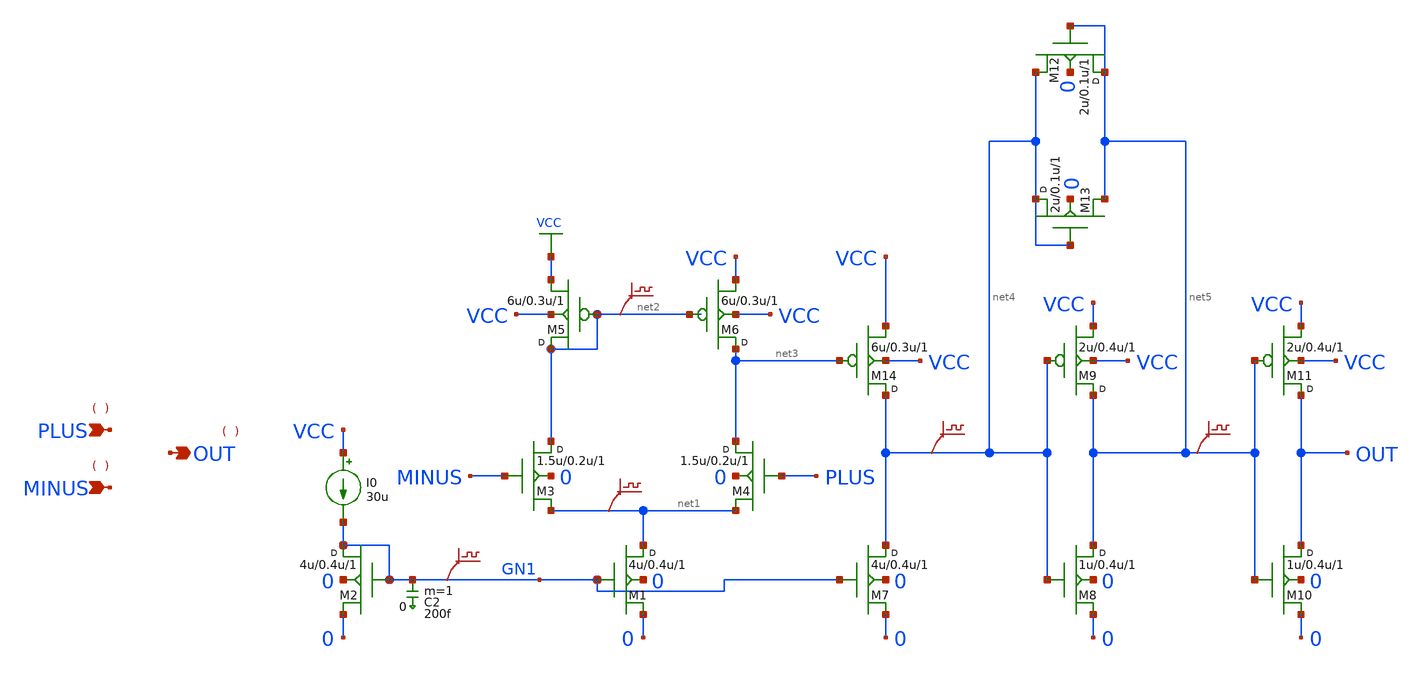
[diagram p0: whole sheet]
** sch_path: xschem-src/xschem_library/inst_sch_select/comp3.sch
* Copyright (C) 1998-2026 Stefan Frederik Schippers
* This program is free software; you can redistribute it and/or modify
* it under the terms of the GNU General Public License as published by
* the Free Software Foundation; either version 2 of the License, or
* (at your option) any later version.
* This program is distributed in the hope that it will be useful,
* but WITHOUT ANY WARRANTY; without even the implied warranty of
* MERCHANTABILITY or FITNESS FOR A PARTICULAR PURPOSE.  See the
* GNU General Public License for more details.
* You should have received a copy of the GNU General Public License
* along with this program; if not, write to the Free Software
**.subckt comp3 PLUS MINUS OUT
*.ipin PLUS
*.ipin MINUS
*.opin OUT
M1 net1 GN1 0 0 nmos w=4u l=0.4u m=1
M2 GN1 GN1 0 0 nmos w=4u l=0.4u m=1
I0 VCC GN1 30u
M3 net2 MINUS net1 0 nmos w=1.5u l=0.2u m=1
M4 net3 PLUS net1 0 nmos w=1.5u l=0.2u m=1
M5 net2 net2 VCC VCC pmos w=6u l=0.3u m=1
M6 net3 net2 VCC VCC pmos w=6u l=0.3u m=1
M14 net4 net3 VCC VCC pmos w=6u l=0.3u m=1
.save v(gn1)
.save v(net2)
M7 net4 GN1 0 0 nmos w=4u l=0.4u m=1
M8 net5 net4 0 0 nmos w=1u l=0.4u m=1
M9 net5 net4 VCC VCC pmos w=2u l=0.4u m=1
M10 OUT net5 0 0 nmos w=1u l=0.4u m=1
M11 OUT net5 VCC VCC pmos w=2u l=0.4u m=1
M13 net4 net4 net5 0 nmos w=2u l=0.1u m=1
.save v(net5)
.save v(net4)
M12 net5 net5 net4 0 nmos w=2u l=0.1u m=1
.save v(net1)
C2 GN1 0 200f m=1
**.ends
.GLOBAL VCC
.end
